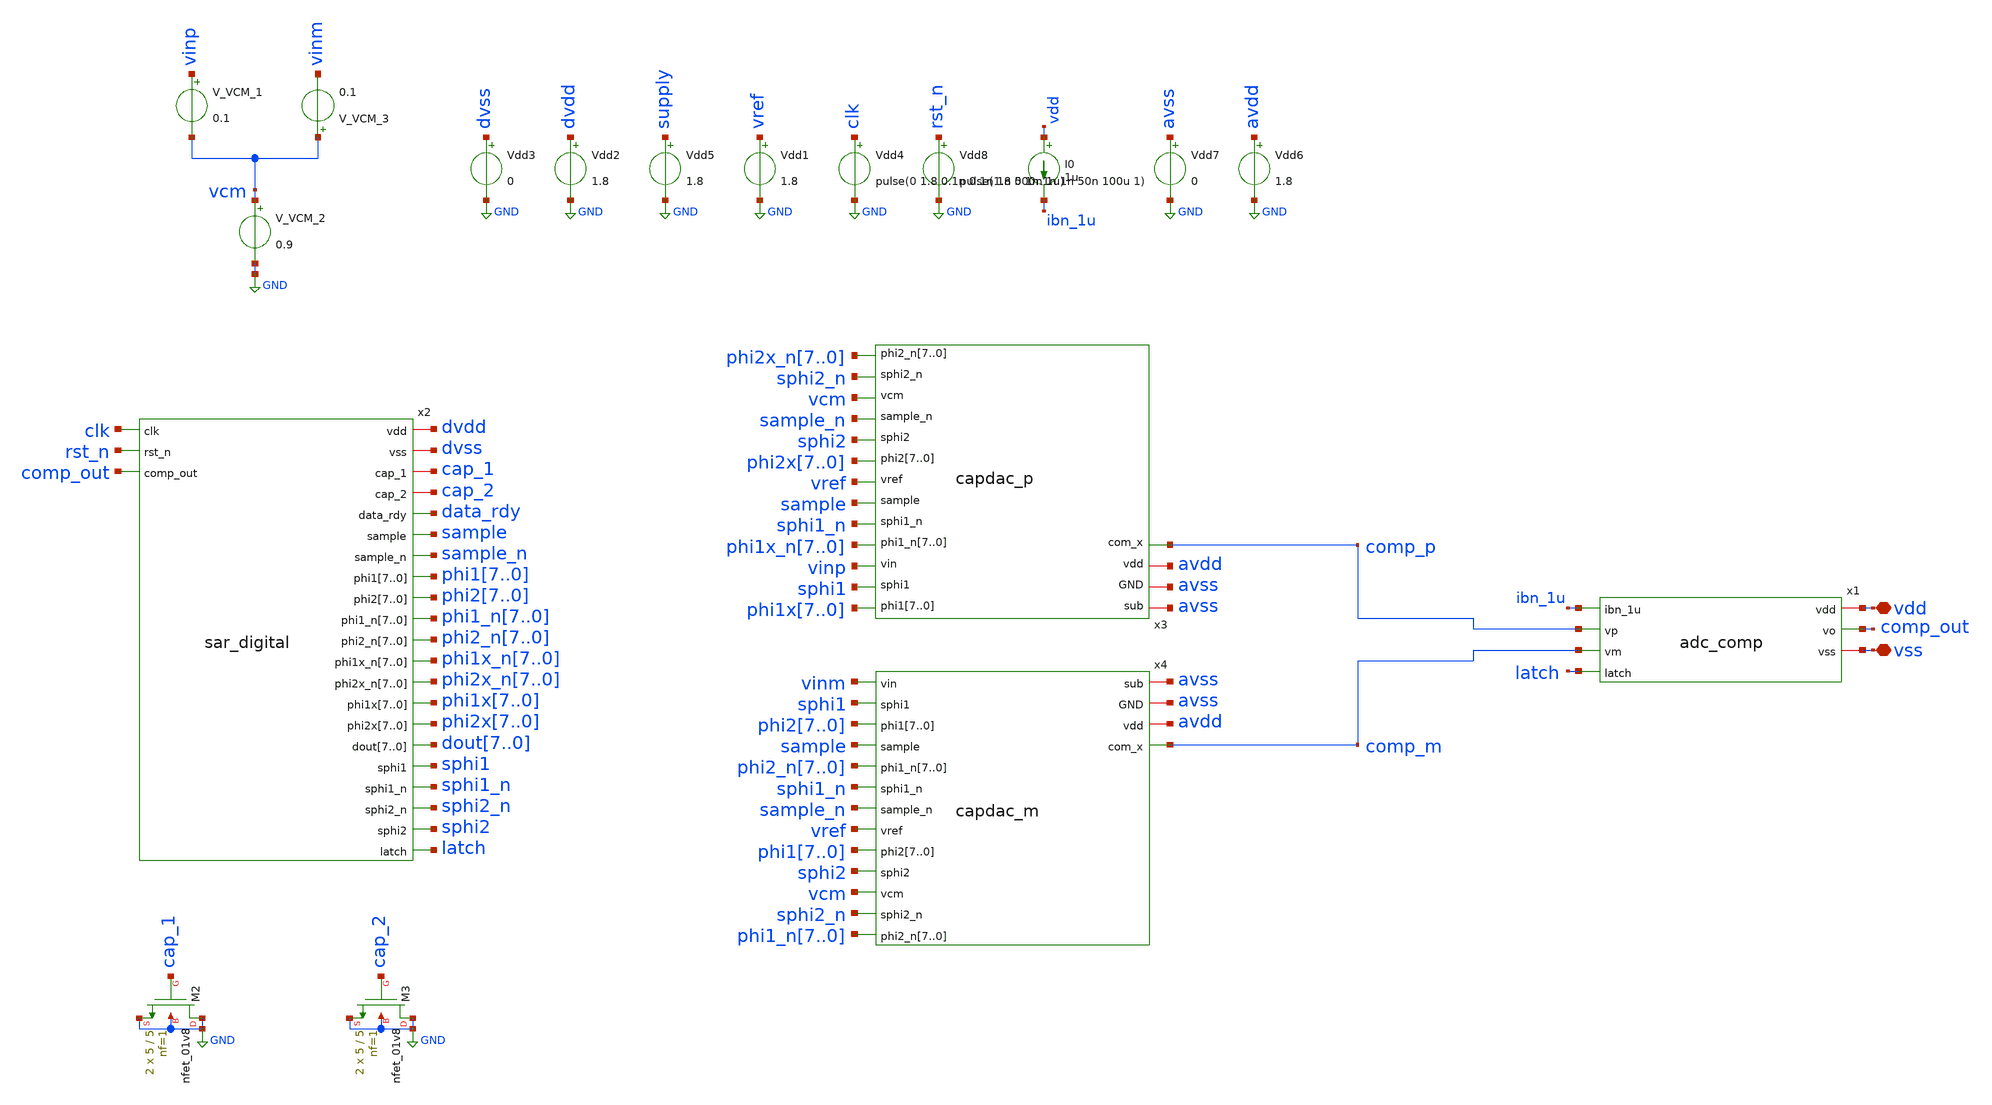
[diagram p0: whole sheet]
** sch_path: test/testbench/sar_tb4.sch
.lib $::SKYWATER_MODELS/sky130.lib.spice tt
.include $::SKYWATER_STDCELLS/sky130_fd_sc_hd.spice

**.subckt sar_tb4 vdd vss
*.iopin vdd
*.iopin vss
Vdd8 rst_n GND pulse(1.8 0 1n 1n 1n 50n 100u 1)
Vdd4 clk GND pulse(0 1.8 0.1n 0.1n 1n 500n 1u)
Vdd1 vref GND 1.8
Vdd5 supply GND 1.8
V_VCM_2 vcm GND 0.9
V_VCM_1 vinp vcm 0.1
V_VCM_3 vcm vinm 0.1
x1 vdd comp_out ibn_1u comp_p comp_m vss latch adc_comp
I0 vdd ibn_1u 1u
XM2 GND cap_1 GND GND sky130_fd_pr__nfet_01v8 L=5 W=5 nf=1 ad='int((nf+1)/2) * W/nf * 0.29' as='int((nf+2)/2) * W/nf * 0.29'
+ pd='2*int((nf+1)/2) * (W/nf + 0.29)' ps='2*int((nf+2)/2) * (W/nf + 0.29)' nrd='0.29 / W' nrs='0.29 / W'
+ sa=0 sb=0 sd=0 mult=2 m=2
XM3 GND cap_2 GND GND sky130_fd_pr__nfet_01v8 L=5 W=5 nf=1 ad='int((nf+1)/2) * W/nf * 0.29' as='int((nf+2)/2) * W/nf * 0.29'
+ pd='2*int((nf+1)/2) * (W/nf + 0.29)' ps='2*int((nf+2)/2) * (W/nf + 0.29)' nrd='0.29 / W' nrs='0.29 / W'
+ sa=0 sb=0 sd=0 mult=2 m=2
x3 phi1x7 phi1x6 phi1x5 phi1x4 phi1x3 phi1x2 phi1x1 phi1x0 sphi1 avss vinp phi1x_n7 phi1x_n6
+ phi1x_n5 phi1x_n4 phi1x_n3 phi1x_n2 phi1x_n1 phi1x_n0 sphi1_n avss sample vref phi2x7 phi2x6 phi2x5 phi2x4
+ phi2x3 phi2x2 phi2x1 phi2x0 sphi2 avdd sample_n vcm sphi2_n phi2x_n7 phi2x_n6 phi2x_n5 phi2x_n4 phi2x_n3
+ phi2x_n2 phi2x_n1 phi2x_n0 comp_p capdac_p
x4 vinm sphi1 phi27 phi26 phi25 phi24 phi23 phi22 phi21 phi20 avss sample phi2_n7 phi2_n6 phi2_n5
+ phi2_n4 phi2_n3 phi2_n2 phi2_n1 phi2_n0 sphi1_n sample_n avss vref phi17 phi16 phi15 phi14 phi13 phi12
+ phi11 phi10 sphi2 avdd vcm sphi2_n phi1_n7 phi1_n6 phi1_n5 phi1_n4 phi1_n3 phi1_n2 phi1_n1 phi1_n0 comp_m
+ capdac_m
x2 dvdd clk rst_n dvss comp_out cap_1 cap_2 data_rdy sample sample_n phi17 phi16 phi15 phi14 phi13
+ phi12 phi11 phi10 phi27 phi26 phi25 phi24 phi23 phi22 phi21 phi20 phi1_n7 phi1_n6 phi1_n5 phi1_n4 phi1_n3
+ phi1_n2 phi1_n1 phi1_n0 phi2_n7 phi2_n6 phi2_n5 phi2_n4 phi2_n3 phi2_n2 phi2_n1 phi2_n0 phi1x_n7 phi1x_n6
+ phi1x_n5 phi1x_n4 phi1x_n3 phi1x_n2 phi1x_n1 phi1x_n0 phi2x_n7 phi2x_n6 phi2x_n5 phi2x_n4 phi2x_n3 phi2x_n2
+ phi2x_n1 phi2x_n0 phi1x7 phi1x6 phi1x5 phi1x4 phi1x3 phi1x2 phi1x1 phi1x0 phi2x7 phi2x6 phi2x5 phi2x4 phi2x3
+ phi2x2 phi2x1 phi2x0 dout7 dout6 dout5 dout4 dout3 dout2 dout1 dout0 sphi1 sphi1_n sphi2_n sphi2 latch
+ sar_digital
Vdd2 dvdd GND 1.8
Vdd3 dvss GND 0
Vdd6 avdd GND 1.8
Vdd7 avss GND 0
**** begin user architecture code


.tran 10n 10u
.save all
.param vcc = 1.8
.param vdd = 1.8
.param vdiff = 200m
vvcc vcc 0 dc vcc
vvdd vdd 0 dc vdd
vvss vss 0 0
.control

run
plot comp_p comp_m
plot dout0+2 dout1+4 dout2+6 dout3+8 dout4+10 dout5+12 dout6+14 dout7+16 data_rdy+18
plot x2.net21 x2.net2+2 x2.net10+4 x2.net19+6
write sar_tb4.raw comp_p comp_m
set wr_singlescale
set wr_vecnames
wrdata sar_tb4.txt comp_p comp_m dout0 dout1 dout2 dout3 dout4 dout5 dout6 dout7 data_rdy vinp vinm
.endc



.model SWITCH1 sw vt=0.9 vh=0 ron=1 roff =100G

**** end user architecture code
**.ends
.GLOBAL GND
.end
